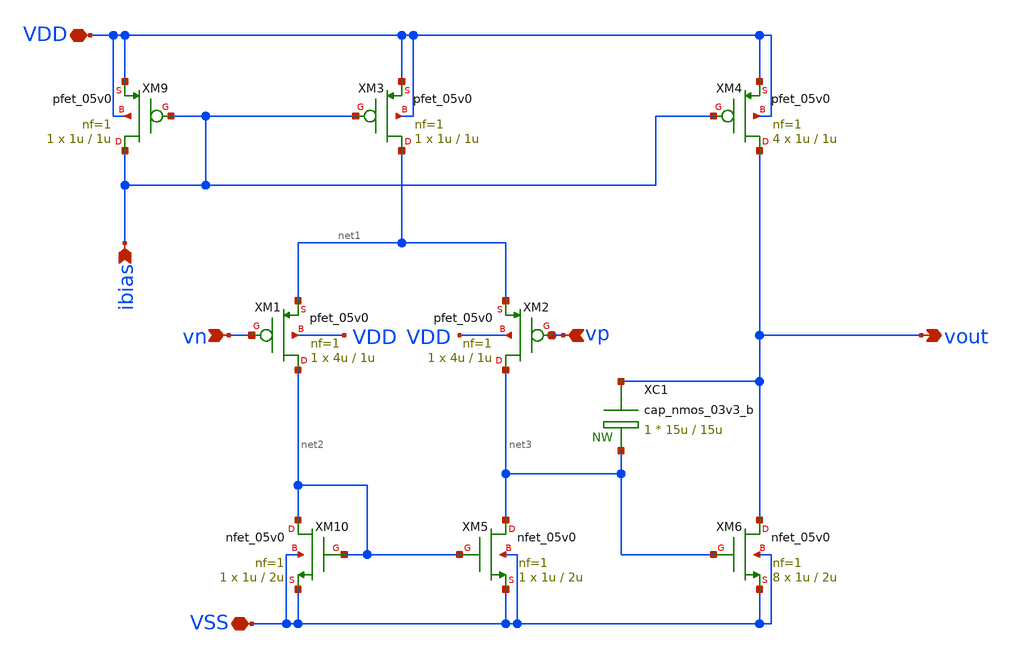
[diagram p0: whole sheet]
** sch_path: designs/libs/core_bandgap/bandgap_opamp/bandgap_opamp.sch
**.subckt bandgap_opamp vn vp vout ibias VDD VSS
*.ipin vn
*.ipin vp
*.opin vout
*.ipin ibias
*.iopin VDD
*.iopin VSS
XC1 vout net3 cap_nmos_03v3_b c_width=15u c_length=15u m=1
XM9 ibias ibias VDD VDD pfet_05v0 L=1u W=1u nf=1 ad='int((nf+1)/2) * W/nf * 0.18u' as='int((nf+2)/2) * W/nf * 0.18u'
+ pd='2*int((nf+1)/2) * (W/nf + 0.18u)' ps='2*int((nf+2)/2) * (W/nf + 0.18u)' nrd='0.18u / W' nrs='0.18u / W'
+ sa=0 sb=0 sd=0 m=1
XM10 net2 net2 VSS VSS nfet_05v0 L=2u W=1u nf=1 ad='int((nf+1)/2) * W/nf * 0.18u' as='int((nf+2)/2) * W/nf * 0.18u'
+ pd='2*int((nf+1)/2) * (W/nf + 0.18u)' ps='2*int((nf+2)/2) * (W/nf + 0.18u)' nrd='0.18u / W' nrs='0.18u / W'
+ sa=0 sb=0 sd=0 m=1
XM3 net1 ibias VDD VDD pfet_05v0 L=1u W=1u nf=1 ad='int((nf+1)/2) * W/nf * 0.18u' as='int((nf+2)/2) * W/nf * 0.18u'
+ pd='2*int((nf+1)/2) * (W/nf + 0.18u)' ps='2*int((nf+2)/2) * (W/nf + 0.18u)' nrd='0.18u / W' nrs='0.18u / W'
+ sa=0 sb=0 sd=0 m=1
XM4 vout ibias VDD VDD pfet_05v0 L=1u W=1u nf=1 ad='int((nf+1)/2) * W/nf * 0.18u' as='int((nf+2)/2) * W/nf * 0.18u'
+ pd='2*int((nf+1)/2) * (W/nf + 0.18u)' ps='2*int((nf+2)/2) * (W/nf + 0.18u)' nrd='0.18u / W' nrs='0.18u / W'
+ sa=0 sb=0 sd=0 m=4
XM1 net2 vn net1 VDD pfet_05v0 L=1u W=4u nf=1 ad='int((nf+1)/2) * W/nf * 0.18u' as='int((nf+2)/2) * W/nf * 0.18u'
+ pd='2*int((nf+1)/2) * (W/nf + 0.18u)' ps='2*int((nf+2)/2) * (W/nf + 0.18u)' nrd='0.18u / W' nrs='0.18u / W'
+ sa=0 sb=0 sd=0 m=1
XM2 net3 vp net1 VDD pfet_05v0 L=1u W=4u nf=1 ad='int((nf+1)/2) * W/nf * 0.18u' as='int((nf+2)/2) * W/nf * 0.18u'
+ pd='2*int((nf+1)/2) * (W/nf + 0.18u)' ps='2*int((nf+2)/2) * (W/nf + 0.18u)' nrd='0.18u / W' nrs='0.18u / W'
+ sa=0 sb=0 sd=0 m=1
XM5 net3 net2 VSS VSS nfet_05v0 L=2u W=1u nf=1 ad='int((nf+1)/2) * W/nf * 0.18u' as='int((nf+2)/2) * W/nf * 0.18u'
+ pd='2*int((nf+1)/2) * (W/nf + 0.18u)' ps='2*int((nf+2)/2) * (W/nf + 0.18u)' nrd='0.18u / W' nrs='0.18u / W'
+ sa=0 sb=0 sd=0 m=1
XM6 vout net3 VSS VSS nfet_05v0 L=2u W=1u nf=1 ad='int((nf+1)/2) * W/nf * 0.18u' as='int((nf+2)/2) * W/nf * 0.18u'
+ pd='2*int((nf+1)/2) * (W/nf + 0.18u)' ps='2*int((nf+2)/2) * (W/nf + 0.18u)' nrd='0.18u / W' nrs='0.18u / W'
+ sa=0 sb=0 sd=0 m=8
**.ends
.end
